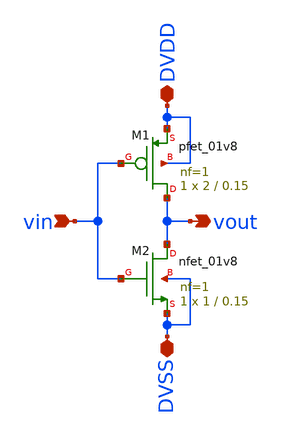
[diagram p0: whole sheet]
** sch_path: xschem/inverter/inv1.sch
**.subckt inv1 vin vout DVDD DVSS
*.ipin vin
*.opin vout
*.iopin DVDD
*.iopin DVSS
XM1 vout vin DVDD DVDD sky130_fd_pr__pfet_01v8 L=0.15 W=2 nf=1 ad='int((nf+1)/2) * W/nf * 0.29' as='int((nf+2)/2) * W/nf * 0.29'
+ pd='2*int((nf+1)/2) * (W/nf + 0.29)' ps='2*int((nf+2)/2) * (W/nf + 0.29)' nrd='0.29 / W' nrs='0.29 / W'
+ sa=0 sb=0 sd=0 mult=1 m=1
XM2 vout vin DVSS DVSS sky130_fd_pr__nfet_01v8 L=0.15 W=1 nf=1 ad='int((nf+1)/2) * W/nf * 0.29' as='int((nf+2)/2) * W/nf * 0.29'
+ pd='2*int((nf+1)/2) * (W/nf + 0.29)' ps='2*int((nf+2)/2) * (W/nf + 0.29)' nrd='0.29 / W' nrs='0.29 / W'
+ sa=0 sb=0 sd=0 mult=1 m=1
**.ends
.end
